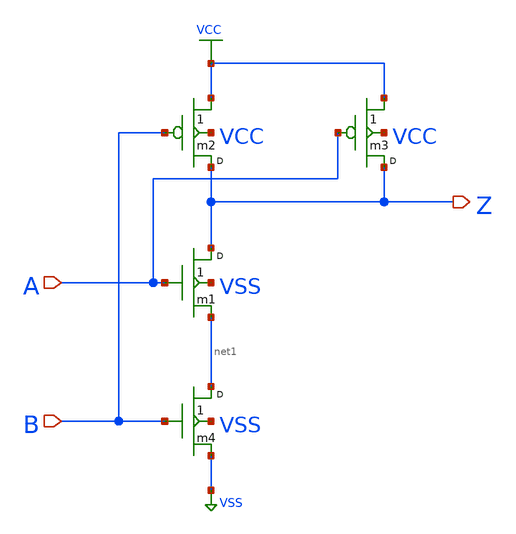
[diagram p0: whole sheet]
** sch_path: library/mylib/nand2.sch
**.subckt nand2 A Z B
*.ipin A
*.opin Z
*.ipin B
m1 Z A net1 VSS nmos w=5u l=0.18u m=1
m2 Z B VCC VCC pmos w=8u l=0.18u m=1
m3 Z A VCC VCC pmos w=8u l=0.18u m=1
m4 net1 B VSS VSS nmos w=5u l=0.18u m=1
**.ends
.GLOBAL VCC
.GLOBAL VSS
.end
